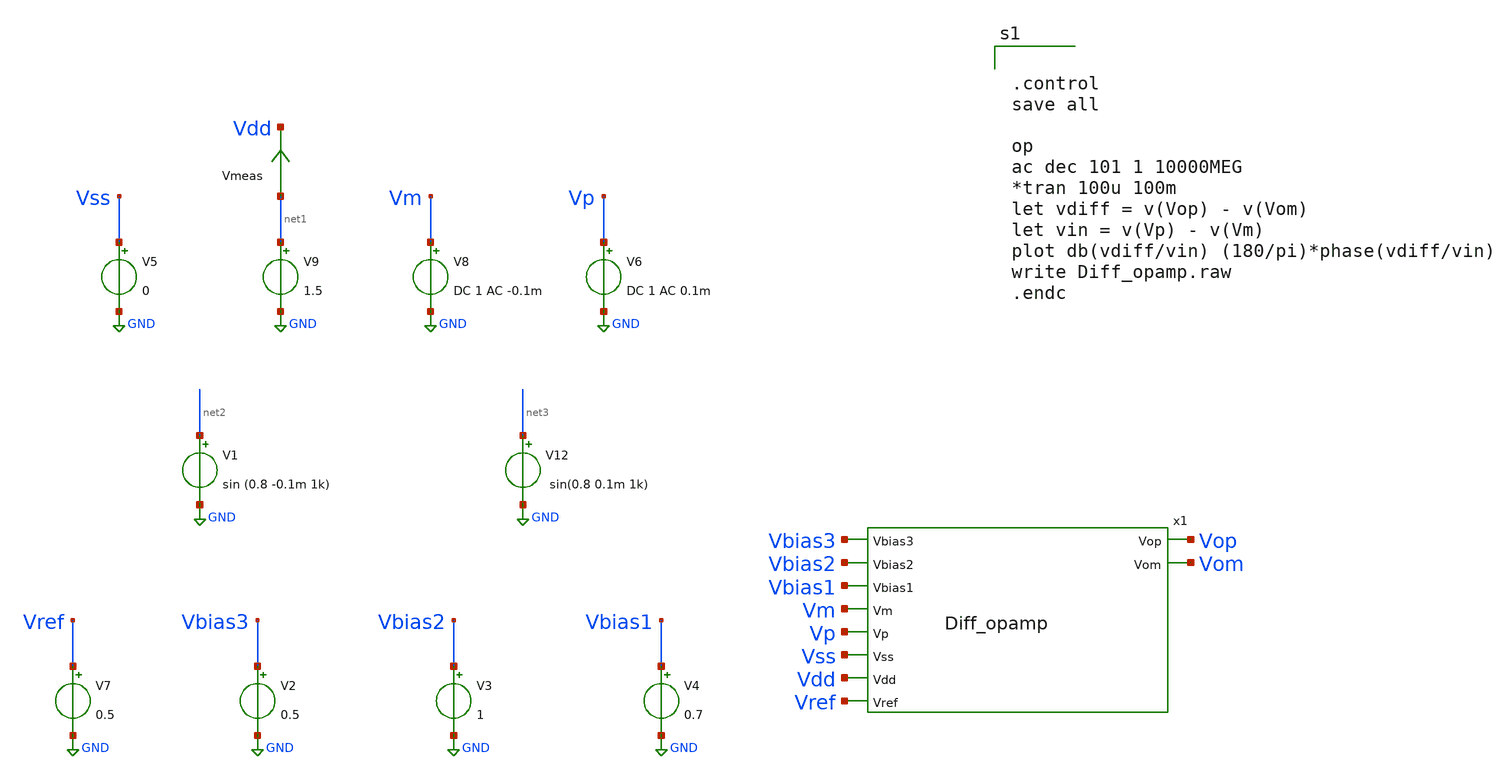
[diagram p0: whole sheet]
** sch_path: src/Opamp_Design/testbenches/Diff_opamp_tb.sch
**.subckt Diff_opamp_tb
x1 Vbias3 Vbias2 Vbias1 Vm Vp Vss Vdd Vref Vop Vom Diff_opamp
V8 Vm GND DC 1 AC -0.1m
V6 Vp GND DC 1 AC 0.1m
V9 net1 GND 1.5
Vmeas net1 Vdd 0
.save i(vmeas)
V1 net2 GND sin (0.8 -0.1m 1k)
V12 net3 GND sin(0.8 0.1m 1k)
V2 Vbias3 GND 0.5
V3 Vbias2 GND 1
V4 Vbias1 GND 0.7
V5 Vss GND 0
V7 Vref GND 0.5
**** begin user architecture code

** opencircuitdesign pdks install
.lib $::SKYWATER_MODELS/sky130.lib.spice tt




.control
save all

op
ac dec 101 1 10000MEG
*tran 100u 100m
let vdiff = v(Vop) - v(Vom)
let vin = v(Vp) - v(Vm)
plot db(vdiff/vin) (180/pi)*phase(vdiff/vin)
write Diff_opamp.raw
.endc


**** end user architecture code
**.ends

* expanding   symbol:  /foss/designs/FYP/Sky130_Multiplier/Opamp_Design/src/Diff_opamp.sym # of
*+ pins=10
** sym_path: src/Opamp_Design/src/Diff_opamp.sym
** sch_path: src/Opamp_Design/src/Diff_opamp.sch
.subckt Diff_opamp Vbias3 Vbias2 Vbias1 Vm Vp Vss Vdd Vref Vop Vom
*.ipin Vss
*.opin Vop
*.ipin Vdd
*.ipin Vp
*.ipin Vm
*.ipin Vref
*.opin Vom
*.ipin Vbias1
*.ipin Vbias2
*.ipin Vbias3
XM5 Vtest2 Vm net2 Vss sky130_fd_pr__nfet_01v8_lvt L=4 W=4 nf=1 ad='int((nf+1)/2) * W/nf * 0.29' as='int((nf+2)/2) * W/nf * 0.29'
+ pd='2*int((nf+1)/2) * (W/nf + 0.29)' ps='2*int((nf+2)/2) * (W/nf + 0.29)' nrd='0.29 / W' nrs='0.29 / W'
+ sa=0 sb=0 sd=0 mult=2 m=2
XM6 net1 Vp net2 Vss sky130_fd_pr__nfet_01v8_lvt L=4 W=4 nf=1 ad='int((nf+1)/2) * W/nf * 0.29' as='int((nf+2)/2) * W/nf * 0.29'
+ pd='2*int((nf+1)/2) * (W/nf + 0.29)' ps='2*int((nf+2)/2) * (W/nf + 0.29)' nrd='0.29 / W' nrs='0.29 / W'
+ sa=0 sb=0 sd=0 mult=2 m=2
XM11 Vop Vbias Vtest2 Vdd sky130_fd_pr__pfet_01v8_lvt L=5 W=2 nf=1 ad='int((nf+1)/2) * W/nf * 0.29' as='int((nf+2)/2) * W/nf * 0.29'
+ pd='2*int((nf+1)/2) * (W/nf + 0.29)' ps='2*int((nf+2)/2) * (W/nf + 0.29)' nrd='0.29 / W' nrs='0.29 / W'
+ sa=0 sb=0 sd=0 mult=2 m=2
XM12 Vom Vbias net1 Vdd sky130_fd_pr__pfet_01v8_lvt L=5 W=2 nf=1 ad='int((nf+1)/2) * W/nf * 0.29' as='int((nf+2)/2) * W/nf * 0.29'
+ pd='2*int((nf+1)/2) * (W/nf + 0.29)' ps='2*int((nf+2)/2) * (W/nf + 0.29)' nrd='0.29 / W' nrs='0.29 / W'
+ sa=0 sb=0 sd=0 mult=2 m=2
XM13 Vtest2 Vout Vdd Vdd sky130_fd_pr__pfet_01v8_lvt L=5 W=2 nf=1 ad='int((nf+1)/2) * W/nf * 0.29' as='int((nf+2)/2) * W/nf * 0.29'
+ pd='2*int((nf+1)/2) * (W/nf + 0.29)' ps='2*int((nf+2)/2) * (W/nf + 0.29)' nrd='0.29 / W' nrs='0.29 / W'
+ sa=0 sb=0 sd=0 mult=4 m=4
XM14 net1 Vout Vdd Vdd sky130_fd_pr__pfet_01v8_lvt L=5 W=2 nf=1 ad='int((nf+1)/2) * W/nf * 0.29' as='int((nf+2)/2) * W/nf * 0.29'
+ pd='2*int((nf+1)/2) * (W/nf + 0.29)' ps='2*int((nf+2)/2) * (W/nf + 0.29)' nrd='0.29 / W' nrs='0.29 / W'
+ sa=0 sb=0 sd=0 mult=4 m=4
XM19 net2 Vbias2 net3 Vss sky130_fd_pr__nfet_01v8_lvt L=1 W=1 nf=1 ad='int((nf+1)/2) * W/nf * 0.29' as='int((nf+2)/2) * W/nf * 0.29'
+ pd='2*int((nf+1)/2) * (W/nf + 0.29)' ps='2*int((nf+2)/2) * (W/nf + 0.29)' nrd='0.29 / W' nrs='0.29 / W'
+ sa=0 sb=0 sd=0 mult=2 m=2
XM1 net3 Vbias1 Vss Vss sky130_fd_pr__nfet_01v8_lvt L=10 W=1 nf=1 ad='int((nf+1)/2) * W/nf * 0.29' as='int((nf+2)/2) * W/nf * 0.29'
+ pd='2*int((nf+1)/2) * (W/nf + 0.29)' ps='2*int((nf+2)/2) * (W/nf + 0.29)' nrd='0.29 / W' nrs='0.29 / W'
+ sa=0 sb=0 sd=0 mult=2 m=2
XM2 net4 Vbias1 Vss Vss sky130_fd_pr__nfet_01v8_lvt L=10 W=1 nf=1 ad='int((nf+1)/2) * W/nf * 0.29' as='int((nf+2)/2) * W/nf * 0.29'
+ pd='2*int((nf+1)/2) * (W/nf + 0.29)' ps='2*int((nf+2)/2) * (W/nf + 0.29)' nrd='0.29 / W' nrs='0.29 / W'
+ sa=0 sb=0 sd=0 mult=2 m=2
XM3 net2 Vbias2 net4 Vss sky130_fd_pr__nfet_01v8_lvt L=1 W=1 nf=1 ad='int((nf+1)/2) * W/nf * 0.29' as='int((nf+2)/2) * W/nf * 0.29'
+ pd='2*int((nf+1)/2) * (W/nf + 0.29)' ps='2*int((nf+2)/2) * (W/nf + 0.29)' nrd='0.29 / W' nrs='0.29 / W'
+ sa=0 sb=0 sd=0 mult=2 m=2
XM4 Vop Vbias2 net5 Vss sky130_fd_pr__nfet_01v8_lvt L=1 W=1 nf=1 ad='int((nf+1)/2) * W/nf * 0.29' as='int((nf+2)/2) * W/nf * 0.29'
+ pd='2*int((nf+1)/2) * (W/nf + 0.29)' ps='2*int((nf+2)/2) * (W/nf + 0.29)' nrd='0.29 / W' nrs='0.29 / W'
+ sa=0 sb=0 sd=0 mult=2 m=2
XM7 net5 Vbias1 Vss Vss sky130_fd_pr__nfet_01v8_lvt L=10 W=1 nf=1 ad='int((nf+1)/2) * W/nf * 0.29' as='int((nf+2)/2) * W/nf * 0.29'
+ pd='2*int((nf+1)/2) * (W/nf + 0.29)' ps='2*int((nf+2)/2) * (W/nf + 0.29)' nrd='0.29 / W' nrs='0.29 / W'
+ sa=0 sb=0 sd=0 mult=2 m=2
XM8 Vom Vbias2 net6 Vss sky130_fd_pr__nfet_01v8_lvt L=1 W=1 nf=1 ad='int((nf+1)/2) * W/nf * 0.29' as='int((nf+2)/2) * W/nf * 0.29'
+ pd='2*int((nf+1)/2) * (W/nf + 0.29)' ps='2*int((nf+2)/2) * (W/nf + 0.29)' nrd='0.29 / W' nrs='0.29 / W'
+ sa=0 sb=0 sd=0 mult=2 m=2
XM9 net6 Vbias1 Vss Vss sky130_fd_pr__nfet_01v8_lvt L=10 W=1 nf=1 ad='int((nf+1)/2) * W/nf * 0.29' as='int((nf+2)/2) * W/nf * 0.29'
+ pd='2*int((nf+1)/2) * (W/nf + 0.29)' ps='2*int((nf+2)/2) * (W/nf + 0.29)' nrd='0.29 / W' nrs='0.29 / W'
+ sa=0 sb=0 sd=0 mult=2 m=2
XM10 Vout Vref net8 Vss sky130_fd_pr__nfet_01v8_lvt L=20 W=5 nf=1 ad='int((nf+1)/2) * W/nf * 0.29' as='int((nf+2)/2) * W/nf * 0.29'
+ pd='2*int((nf+1)/2) * (W/nf + 0.29)' ps='2*int((nf+2)/2) * (W/nf + 0.29)' nrd='0.29 / W' nrs='0.29 / W'
+ sa=0 sb=0 sd=0 mult=2 m=2
XM17 net9 Vop net8 Vss sky130_fd_pr__nfet_01v8_lvt L=20 W=5 nf=1 ad='int((nf+1)/2) * W/nf * 0.29' as='int((nf+2)/2) * W/nf * 0.29'
+ pd='2*int((nf+1)/2) * (W/nf + 0.29)' ps='2*int((nf+2)/2) * (W/nf + 0.29)' nrd='0.29 / W' nrs='0.29 / W'
+ sa=0 sb=0 sd=0 mult=2 m=2
XM18 net9 Vom net7 Vss sky130_fd_pr__nfet_01v8_lvt L=20 W=5 nf=1 ad='int((nf+1)/2) * W/nf * 0.29' as='int((nf+2)/2) * W/nf * 0.29'
+ pd='2*int((nf+1)/2) * (W/nf + 0.29)' ps='2*int((nf+2)/2) * (W/nf + 0.29)' nrd='0.29 / W' nrs='0.29 / W'
+ sa=0 sb=0 sd=0 mult=2 m=2
XM22 net7 Vbias1 Vss Vss sky130_fd_pr__nfet_01v8_lvt L=20 W=1 nf=1 ad='int((nf+1)/2) * W/nf * 0.29' as='int((nf+2)/2) * W/nf * 0.29'
+ pd='2*int((nf+1)/2) * (W/nf + 0.29)' ps='2*int((nf+2)/2) * (W/nf + 0.29)' nrd='0.29 / W' nrs='0.29 / W'
+ sa=0 sb=0 sd=0 mult=2 m=2
XM20 net9 net9 Vdd Vdd sky130_fd_pr__pfet_01v8_lvt L=10 W=1 nf=1 ad='int((nf+1)/2) * W/nf * 0.29' as='int((nf+2)/2) * W/nf * 0.29'
+ pd='2*int((nf+1)/2) * (W/nf + 0.29)' ps='2*int((nf+2)/2) * (W/nf + 0.29)' nrd='0.29 / W' nrs='0.29 / W'
+ sa=0 sb=0 sd=0 mult=2 m=2
XM21 Vout net9 Vdd Vdd sky130_fd_pr__pfet_01v8_lvt L=10 W=1 nf=1 ad='int((nf+1)/2) * W/nf * 0.29' as='int((nf+2)/2) * W/nf * 0.29'
+ pd='2*int((nf+1)/2) * (W/nf + 0.29)' ps='2*int((nf+2)/2) * (W/nf + 0.29)' nrd='0.29 / W' nrs='0.29 / W'
+ sa=0 sb=0 sd=0 mult=2 m=2
XM15 net8 Vbias1 Vss Vss sky130_fd_pr__nfet_01v8_lvt L=20 W=1 nf=1 ad='int((nf+1)/2) * W/nf * 0.29' as='int((nf+2)/2) * W/nf * 0.29'
+ pd='2*int((nf+1)/2) * (W/nf + 0.29)' ps='2*int((nf+2)/2) * (W/nf + 0.29)' nrd='0.29 / W' nrs='0.29 / W'
+ sa=0 sb=0 sd=0 mult=2 m=2
XM16 Vout Vref net7 Vss sky130_fd_pr__nfet_01v8_lvt L=20 W=5 nf=1 ad='int((nf+1)/2) * W/nf * 0.29' as='int((nf+2)/2) * W/nf * 0.29'
+ pd='2*int((nf+1)/2) * (W/nf + 0.29)' ps='2*int((nf+2)/2) * (W/nf + 0.29)' nrd='0.29 / W' nrs='0.29 / W'
+ sa=0 sb=0 sd=0 mult=2 m=2
XM46 Vbias1 Vbias1 Vss Vss sky130_fd_pr__nfet_01v8_lvt L=2 W=1 nf=1 ad='int((nf+1)/2) * W/nf * 0.29'
+ as='int((nf+2)/2) * W/nf * 0.29' pd='2*int((nf+1)/2) * (W/nf + 0.29)' ps='2*int((nf+2)/2) * (W/nf + 0.29)'
+ nrd='0.29 / W' nrs='0.29 / W' sa=0 sb=0 sd=0 mult=2 m=2
XM47 Vbias2 Vbias2 Vss Vss sky130_fd_pr__nfet_01v8_lvt L=5 W=0.6 nf=1 ad='int((nf+1)/2) * W/nf * 0.29'
+ as='int((nf+2)/2) * W/nf * 0.29' pd='2*int((nf+1)/2) * (W/nf + 0.29)' ps='2*int((nf+2)/2) * (W/nf + 0.29)'
+ nrd='0.29 / W' nrs='0.29 / W' sa=0 sb=0 sd=0 mult=2 m=2
XM23 Vbias3 Vbias3 Vss Vss sky130_fd_pr__nfet_01v8_lvt L=1 W=0.6 nf=1 ad='int((nf+1)/2) * W/nf * 0.29'
+ as='int((nf+2)/2) * W/nf * 0.29' pd='2*int((nf+1)/2) * (W/nf + 0.29)' ps='2*int((nf+2)/2) * (W/nf + 0.29)'
+ nrd='0.29 / W' nrs='0.29 / W' sa=0 sb=0 sd=0 mult=2 m=2
XM24 Vbias Vbias3 Vss Vss sky130_fd_pr__nfet_01v8_lvt L=1 W=0.6 nf=1 ad='int((nf+1)/2) * W/nf * 0.29'
+ as='int((nf+2)/2) * W/nf * 0.29' pd='2*int((nf+1)/2) * (W/nf + 0.29)' ps='2*int((nf+2)/2) * (W/nf + 0.29)'
+ nrd='0.29 / W' nrs='0.29 / W' sa=0 sb=0 sd=0 mult=2 m=2
XM25 Vbias Vbias Vdd Vdd sky130_fd_pr__pfet_01v8_lvt L=10 W=1.5 nf=1 ad='int((nf+1)/2) * W/nf * 0.29'
+ as='int((nf+2)/2) * W/nf * 0.29' pd='2*int((nf+1)/2) * (W/nf + 0.29)' ps='2*int((nf+2)/2) * (W/nf + 0.29)'
+ nrd='0.29 / W' nrs='0.29 / W' sa=0 sb=0 sd=0 mult=2 m=2
.ends

.GLOBAL GND
.end
